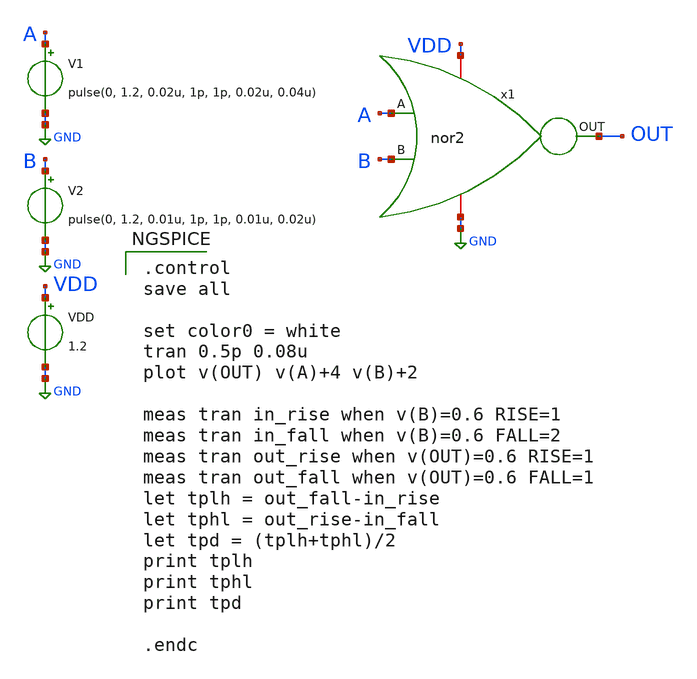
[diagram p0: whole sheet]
** sch_path: design/NOR2/xschem/nor2_tb.sch
**.subckt nor2_tb
V1 A GND pulse(0, 1.2, 0.02u, 1p, 1p, 0.02u, 0.04u)
V2 B GND pulse(0, 1.2, 0.01u, 1p, 1p, 0.01u, 0.02u)
VDD VDD GND 1.2
x1 A B GND VDD OUT nor2
**** begin user architecture code

** opencircuitdesign pdks install
.lib $::SKYWATER_MODELS/sky130.lib.spice tt_mm



.control
save all

set color0 = white
tran 0.5p 0.08u
plot v(OUT) v(A)+4 v(B)+2

meas tran in_rise when v(B)=0.6 RISE=1
meas tran in_fall when v(B)=0.6 FALL=2
meas tran out_rise when v(OUT)=0.6 RISE=1
meas tran out_fall when v(OUT)=0.6 FALL=1
let tplh = out_fall-in_rise
let tphl = out_rise-in_fall
let tpd = (tplh+tphl)/2
print tplh
print tphl
print tpd

.endc

**** end user architecture code
**.ends
.GLOBAL GND
.end
